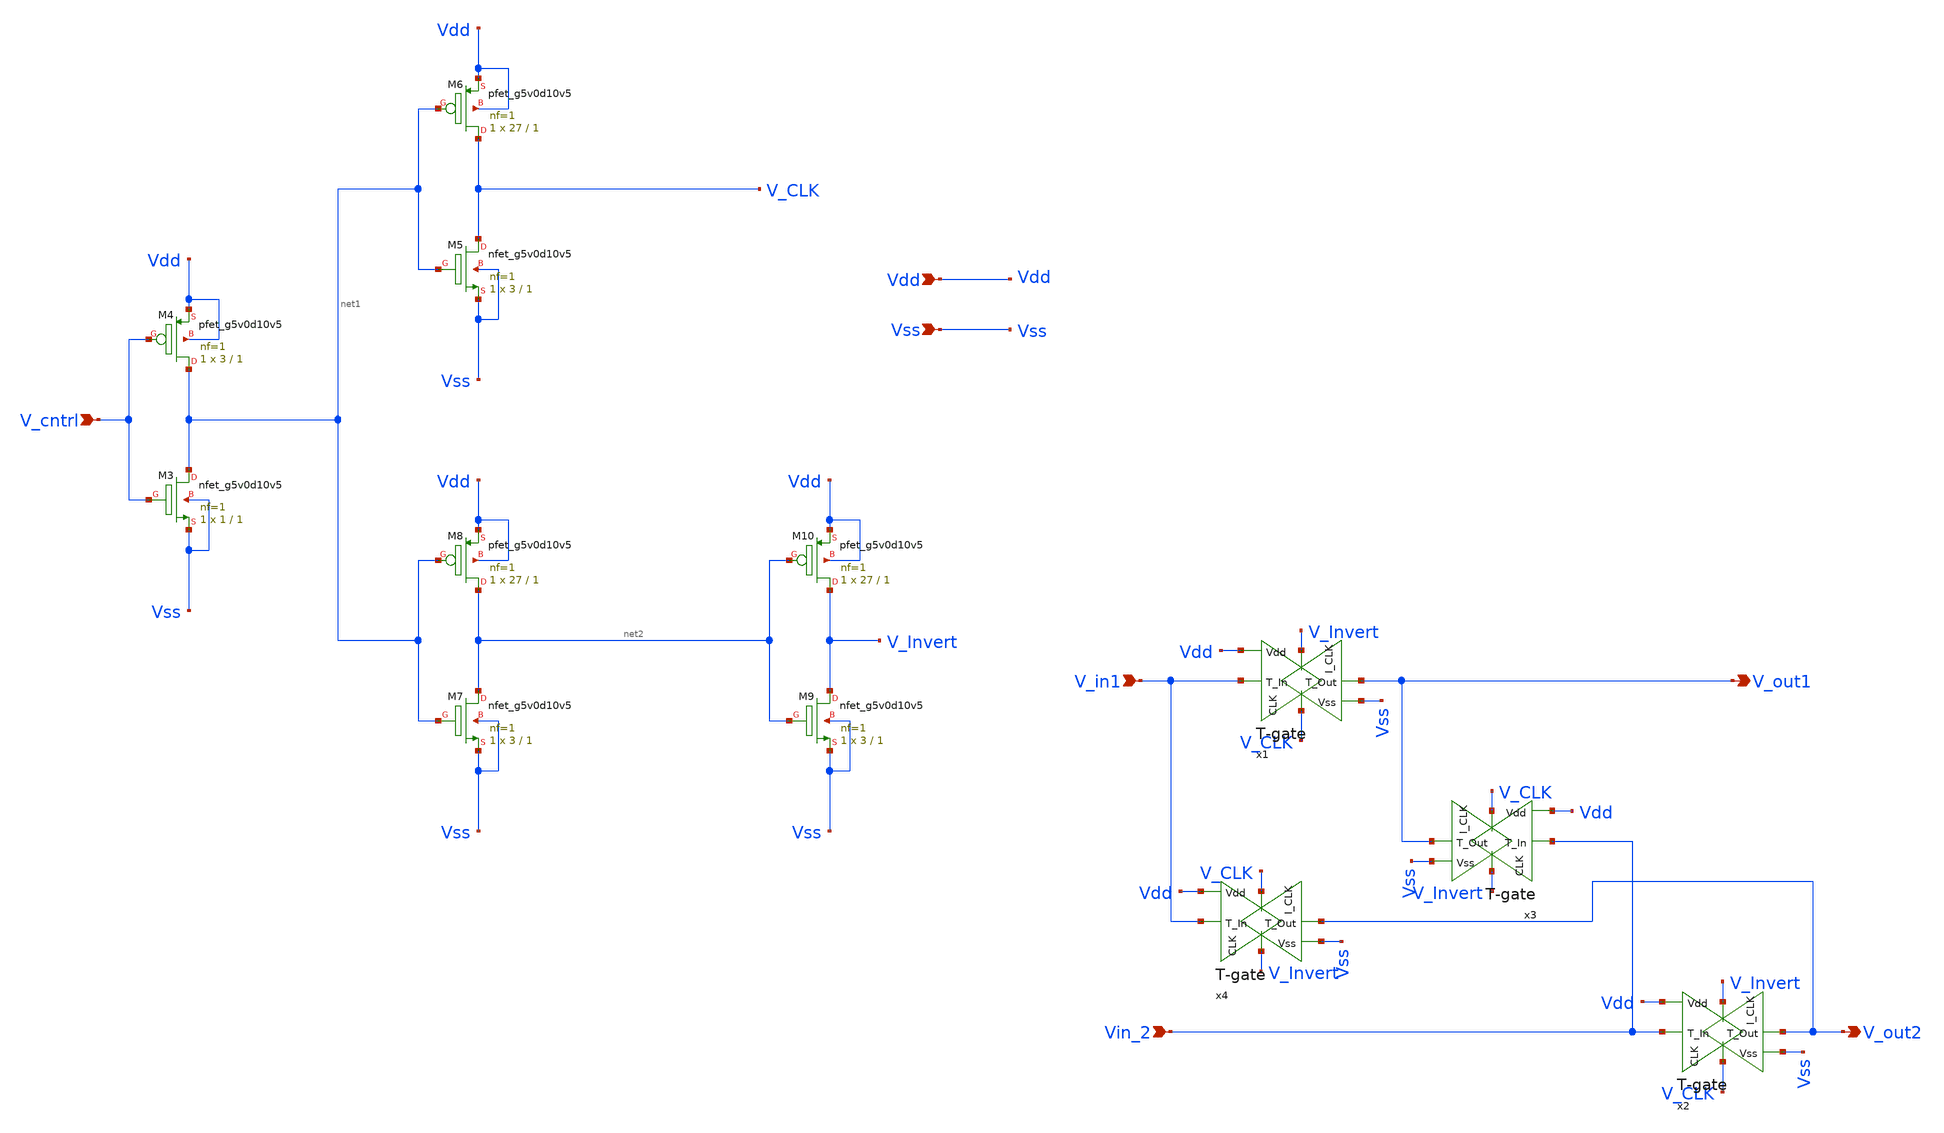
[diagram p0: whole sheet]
** sch_path: xschem/PasMix.sch
**.subckt PasMix V_in1 Vin_2 V_out1 V_out2 Vdd Vss V_cntrl
*.ipin V_in1
*.ipin Vin_2
*.opin V_out1
*.opin V_out2
*.ipin Vdd
*.ipin Vss
*.ipin V_cntrl
x1 V_Invert V_in1 V_out1 Vdd Vss V_CLK T-gate
x2 V_Invert Vin_2 V_out2 Vdd Vss V_CLK T-gate
x3 V_CLK Vin_2 V_out1 Vdd Vss V_Invert T-gate
x4 V_CLK V_in1 V_out2 Vdd Vss V_Invert T-gate
XM3 net1 V_cntrl Vss Vss sky130_fd_pr__nfet_g5v0d10v5 L=1 W=1 nf=1 ad='int((1 + 1)/2) * 1 / 1 * 0.29'
+ as='int((1 + 2)/2) * 1 / 1 * 0.29' pd='2*int((1 + 1)/2) * (1 / 1 + 0.29)' ps='2*int((1 + 2)/2) * (1 / 1 + 0.29)'
+ nrd='0.29 / 1 ' nrs='0.29 / 1 ' sa=0 sb=0 sd=0 mult=1 m=1
XM4 net1 V_cntrl Vdd Vdd sky130_fd_pr__pfet_g5v0d10v5 L=1 W=3 nf=1 ad='int((1 + 1)/2) * 3 / 1 * 0.29'
+ as='int((1 + 2)/2) * 3 / 1 * 0.29' pd='2*int((1 + 1)/2) * (3 / 1 + 0.29)' ps='2*int((1 + 2)/2) * (3 / 1 + 0.29)'
+ nrd='0.29 / 3 ' nrs='0.29 / 3 ' sa=0 sb=0 sd=0 mult=1 m=1
XM5 V_CLK net1 Vss Vss sky130_fd_pr__nfet_g5v0d10v5 L=1 W=3 nf=1 ad='int((1 + 1)/2) * 3 / 1 * 0.29' as='int((1 + 2)/2) * 3 / 1 * 0.29'
+ pd='2*int((1 + 1)/2) * (3 / 1 + 0.29)' ps='2*int((1 + 2)/2) * (3 / 1 + 0.29)' nrd='0.29 / 3 ' nrs='0.29 / 3 '
+ sa=0 sb=0 sd=0 mult=1 m=1
XM6 V_CLK net1 Vdd Vdd sky130_fd_pr__pfet_g5v0d10v5 L=1 W=27 nf=1 ad='int((1 + 1)/2) * 27 / 1 * 0.29'
+ as='int((1 + 2)/2) * 27 / 1 * 0.29' pd='2*int((1 + 1)/2) * (27 / 1 + 0.29)' ps='2*int((1 + 2)/2) * (27 / 1 + 0.29)'
+ nrd='0.29 / 27 ' nrs='0.29 / 27 ' sa=0 sb=0 sd=0 mult=1 m=1
XM7 net2 net1 Vss Vss sky130_fd_pr__nfet_g5v0d10v5 L=1 W=3 nf=1 ad='int((1 + 1)/2) * 3 / 1 * 0.29' as='int((1 + 2)/2) * 3 / 1 * 0.29'
+ pd='2*int((1 + 1)/2) * (3 / 1 + 0.29)' ps='2*int((1 + 2)/2) * (3 / 1 + 0.29)' nrd='0.29 / 3 ' nrs='0.29 / 3 '
+ sa=0 sb=0 sd=0 mult=1 m=1
XM8 net2 net1 Vdd Vdd sky130_fd_pr__pfet_g5v0d10v5 L=1 W=27 nf=1 ad='int((1 + 1)/2) * 27 / 1 * 0.29'
+ as='int((1 + 2)/2) * 27 / 1 * 0.29' pd='2*int((1 + 1)/2) * (27 / 1 + 0.29)' ps='2*int((1 + 2)/2) * (27 / 1 + 0.29)'
+ nrd='0.29 / 27 ' nrs='0.29 / 27 ' sa=0 sb=0 sd=0 mult=1 m=1
XM9 V_Invert net2 Vss Vss sky130_fd_pr__nfet_g5v0d10v5 L=1 W=3 nf=1 ad='int((1 + 1)/2) * 3 / 1 * 0.29'
+ as='int((1 + 2)/2) * 3 / 1 * 0.29' pd='2*int((1 + 1)/2) * (3 / 1 + 0.29)' ps='2*int((1 + 2)/2) * (3 / 1 + 0.29)'
+ nrd='0.29 / 3 ' nrs='0.29 / 3 ' sa=0 sb=0 sd=0 mult=1 m=1
XM10 V_Invert net2 Vdd Vdd sky130_fd_pr__pfet_g5v0d10v5 L=1 W=27 nf=1 ad='int((1 + 1)/2) * 27 / 1 * 0.29'
+ as='int((1 + 2)/2) * 27 / 1 * 0.29' pd='2*int((1 + 1)/2) * (27 / 1 + 0.29)' ps='2*int((1 + 2)/2) * (27 / 1 + 0.29)'
+ nrd='0.29 / 27 ' nrs='0.29 / 27 ' sa=0 sb=0 sd=0 mult=1 m=1
**.ends

* expanding   symbol:  T-gate.sym # of pins=6
** sym_path: xschem/T-gate.sym
** sch_path: xschem/T-gate.sch
.subckt T-gate I_CLK T_In T_Out Vdd Vss CLK
*.ipin T_In
*.opin T_Out
*.ipin Vdd
*.ipin Vss
*.ipin I_CLK
*.ipin CLK
XM1 T_In I_CLK T_Out Vdd sky130_fd_pr__pfet_g5v0d10v5 L=0.5 W=3 nf=1 ad='int((1 + 1)/2) * 3 / 1 * 0.29'
+ as='int((1 + 2)/2) * 3 / 1 * 0.29' pd='2*int((1 + 1)/2) * (3 / 1 + 0.29)' ps='2*int((1 + 2)/2) * (3 / 1 + 0.29)'
+ nrd='0.29 / 3 ' nrs='0.29 / 3 ' sa=0 sb=0 sd=0 mult=1 m=1
XM3 T_Out CLK T_In Vss sky130_fd_pr__nfet_g5v0d10v5 L=0.5 W=1 nf=1 ad='int((1 + 1)/2) * 1 / 1 * 0.29'
+ as='int((1 + 2)/2) * 1 / 1 * 0.29' pd='2*int((1 + 1)/2) * (1 / 1 + 0.29)' ps='2*int((1 + 2)/2) * (1 / 1 + 0.29)'
+ nrd='0.29 / 1 ' nrs='0.29 / 1 ' sa=0 sb=0 sd=0 mult=1 m=1
XM2 T_Out CLK T_Out Vdd sky130_fd_pr__pfet_g5v0d10v5 L=0.5 W=1.5 nf=1 ad='int((1 + 1)/2) * 1.5 / 1 * 0.29'
+ as='int((1 + 2)/2) * 1.5 / 1 * 0.29' pd='2*int((1 + 1)/2) * (1.5 / 1 + 0.29)' ps='2*int((1 + 2)/2) * (1.5 / 1 + 0.29)'
+ nrd='0.29 / 1.5 ' nrs='0.29 / 1.5 ' sa=0 sb=0 sd=0 mult=1 m=1
XM4 T_In CLK T_In Vdd sky130_fd_pr__pfet_g5v0d10v5 L=0.5 W=1.5 nf=1 ad='int((1 + 1)/2) * 1.5 / 1 * 0.29'
+ as='int((1 + 2)/2) * 1.5 / 1 * 0.29' pd='2*int((1 + 1)/2) * (1.5 / 1 + 0.29)' ps='2*int((1 + 2)/2) * (1.5 / 1 + 0.29)'
+ nrd='0.29 / 1.5 ' nrs='0.29 / 1.5 ' sa=0 sb=0 sd=0 mult=1 m=1
XM5 T_In I_CLK T_In Vss sky130_fd_pr__nfet_g5v0d10v5 L=0.5 W=0.5 nf=1 ad='int((1 + 1)/2) * 0.5 / 1 * 0.29'
+ as='int((1 + 2)/2) * 0.5 / 1 * 0.29' pd='2*int((1 + 1)/2) * (0.5 / 1 + 0.29)' ps='2*int((1 + 2)/2) * (0.5 / 1 + 0.29)'
+ nrd='0.29 / 0.5 ' nrs='0.29 / 0.5 ' sa=0 sb=0 sd=0 mult=1 m=1
XM6 T_Out I_CLK T_Out Vss sky130_fd_pr__nfet_g5v0d10v5 L=0.5 W=0.5 nf=1 ad='int((1 + 1)/2) * 0.5 / 1 * 0.29'
+ as='int((1 + 2)/2) * 0.5 / 1 * 0.29' pd='2*int((1 + 1)/2) * (0.5 / 1 + 0.29)' ps='2*int((1 + 2)/2) * (0.5 / 1 + 0.29)'
+ nrd='0.29 / 0.5 ' nrs='0.29 / 0.5 ' sa=0 sb=0 sd=0 mult=1 m=1
.ends

.end
